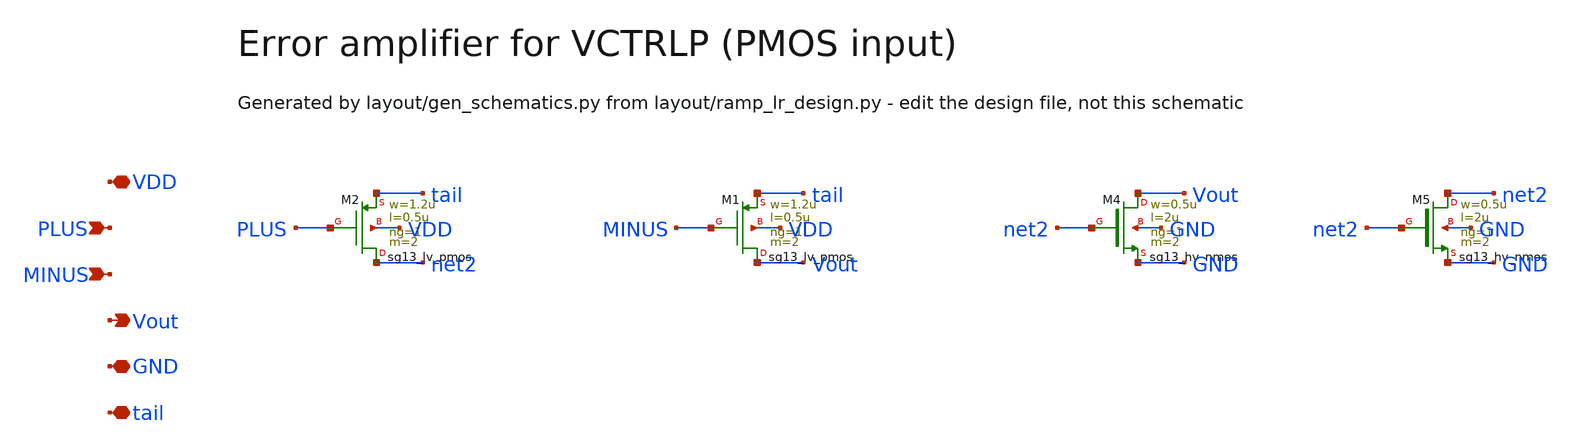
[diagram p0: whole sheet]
** sch_path: Design Files/RAMP/RAMP-LR/POTA_LR.sch
**.subckt POTA_LR VDD PLUS MINUS Vout GND tail
*.iopin VDD
*.ipin PLUS
*.ipin MINUS
*.opin Vout
*.iopin GND
*.iopin tail
XM2 net2 PLUS tail VDD sg13_lv_pmos w=1.2u l=0.5u ng=1 m=2 mm_ok=1
XM1 Vout MINUS tail VDD sg13_lv_pmos w=1.2u l=0.5u ng=1 m=2 mm_ok=1
XM4 Vout net2 GND GND sg13_hv_nmos w=0.5u l=2u ng=1 m=2 mm_ok=1
XM5 net2 net2 GND GND sg13_hv_nmos w=0.5u l=2u ng=1 m=2 mm_ok=1
**.ends
.end
